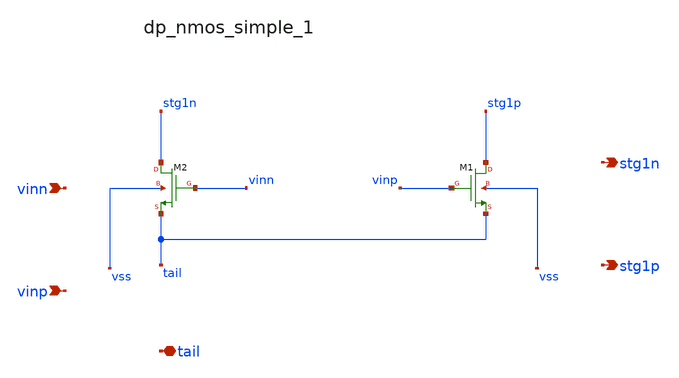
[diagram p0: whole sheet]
** sch_path: analog-db/raw/amp_029_two_stage_miller_comp/hier/blocks/dp_nmos_simple_1.sch
**.subckt dp_nmos_simple_1 vinn vinp tail stg1n stg1p
*.ipin vinn
*.ipin vinp
*.iopin tail
*.opin stg1n
*.opin stg1p
XM1 stg1p vinp tail vss sg13_lv_nmos w=x_dut_xm1_w l=x_dut_xm1_l ng=1 m=x_dut_xm1_m
XM2 stg1n vinn tail vss sg13_lv_nmos w=x_dut_xm2_w l=x_dut_xm2_l ng=1 m=x_dut_xm2_m
**.ends
.end
